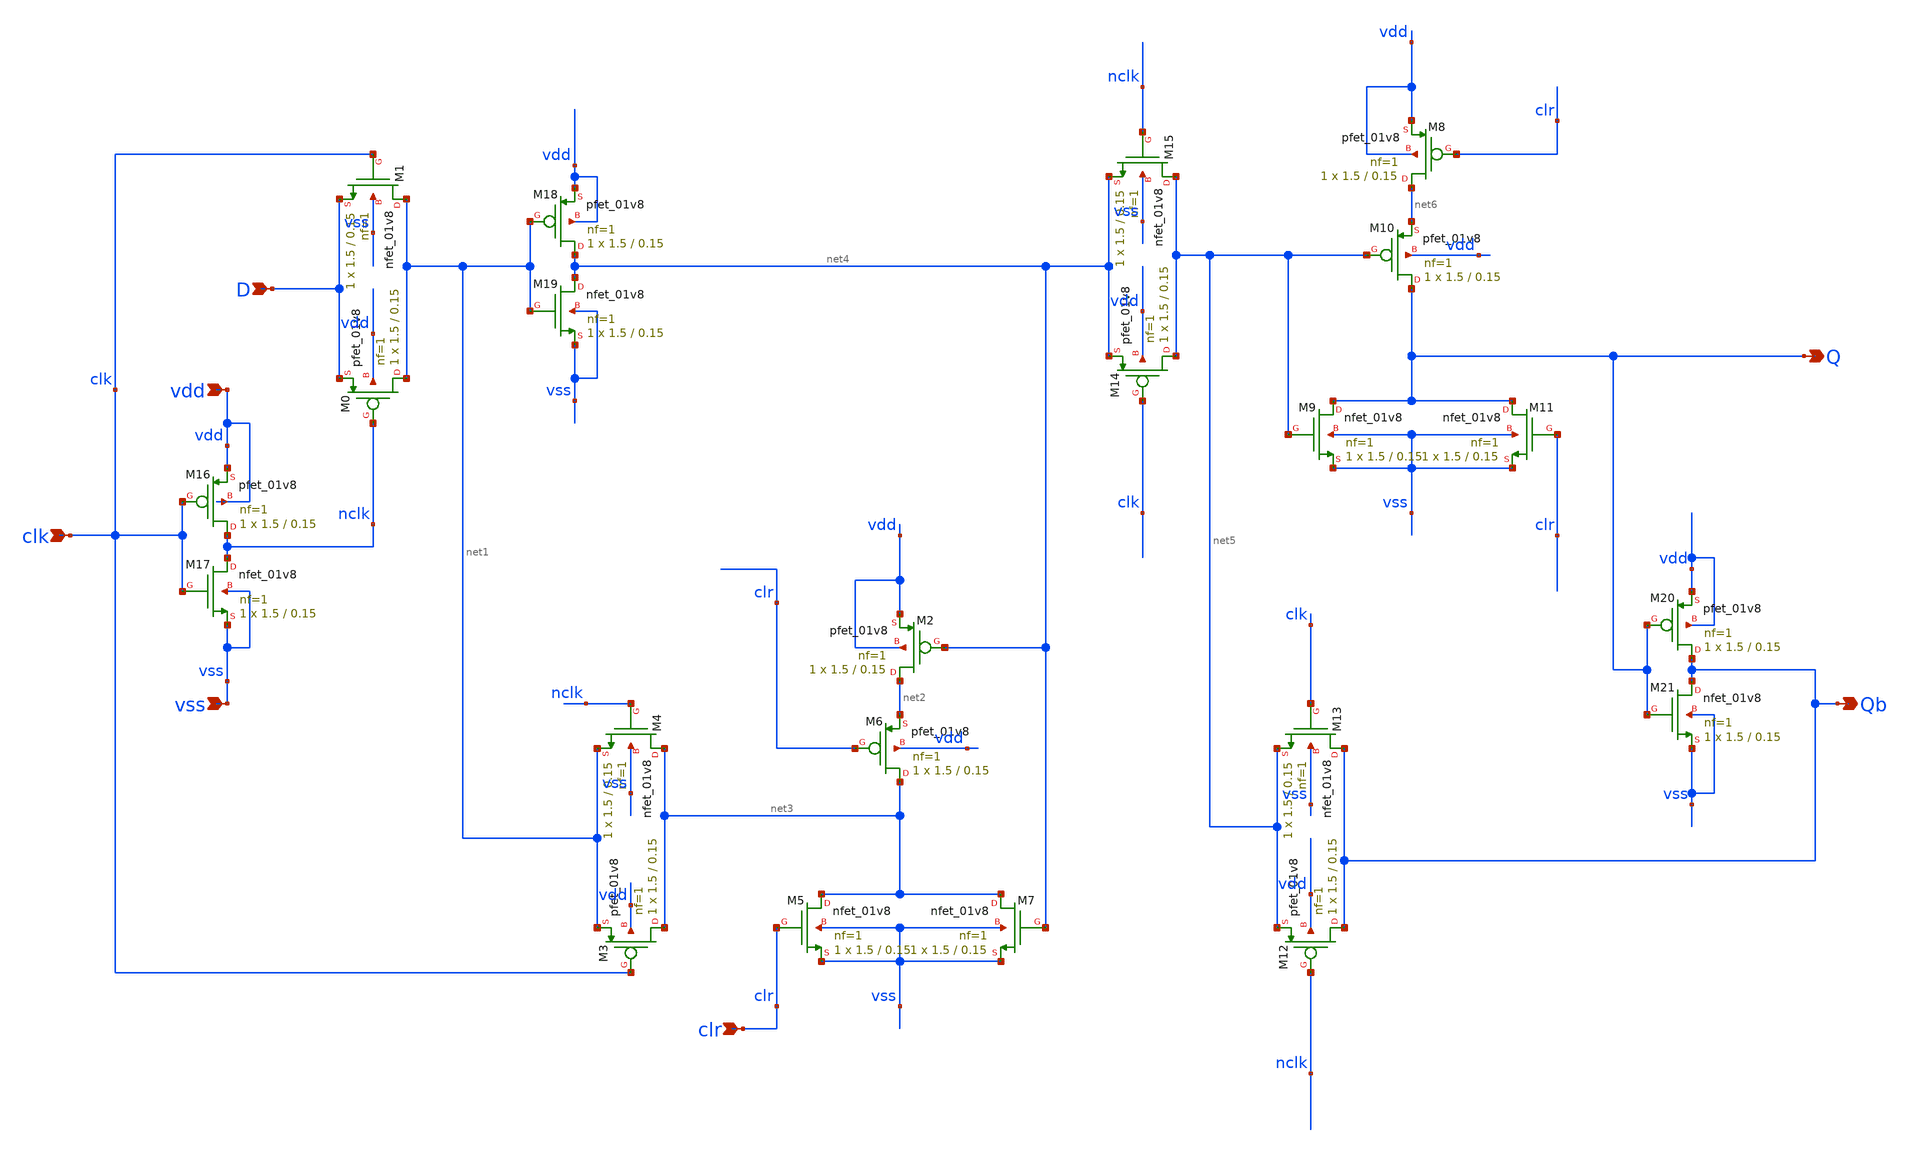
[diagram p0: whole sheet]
** sch_path: track_vlsi/lado/sch/dffc.sch
**.subckt dffc clk vdd vss D Q Qb clr
*.ipin clk
*.ipin vdd
*.ipin vss
*.ipin D
*.opin Q
*.opin Qb
*.ipin clr
XM0 net1 nclk D vdd sky130_fd_pr__pfet_01v8 L=0.15 W=1.5 nf=1 ad='int((nf+1)/2) * W/nf * 0.29' as='int((nf+2)/2) * W/nf * 0.29'
+ pd='2*int((nf+1)/2) * (W/nf + 0.29)' ps='2*int((nf+2)/2) * (W/nf + 0.29)' nrd='0.29 / W' nrs='0.29 / W'
+ sa=0 sb=0 sd=0 mult=1 m=1
XM1 net1 clk D vss sky130_fd_pr__nfet_01v8 L=0.15 W=1.5 nf=1 ad='int((nf+1)/2) * W/nf * 0.29' as='int((nf+2)/2) * W/nf * 0.29'
+ pd='2*int((nf+1)/2) * (W/nf + 0.29)' ps='2*int((nf+2)/2) * (W/nf + 0.29)' nrd='0.29 / W' nrs='0.29 / W'
+ sa=0 sb=0 sd=0 mult=1 m=1
XM2 net2 net4 vdd vdd sky130_fd_pr__pfet_01v8 L=0.15 W=1.5 nf=1 ad='int((nf+1)/2) * W/nf * 0.29' as='int((nf+2)/2) * W/nf * 0.29'
+ pd='2*int((nf+1)/2) * (W/nf + 0.29)' ps='2*int((nf+2)/2) * (W/nf + 0.29)' nrd='0.29 / W' nrs='0.29 / W'
+ sa=0 sb=0 sd=0 mult=1 m=1
XM5 net3 clr vss vss sky130_fd_pr__nfet_01v8 L=0.15 W=1.5 nf=1 ad='int((nf+1)/2) * W/nf * 0.29' as='int((nf+2)/2) * W/nf * 0.29'
+ pd='2*int((nf+1)/2) * (W/nf + 0.29)' ps='2*int((nf+2)/2) * (W/nf + 0.29)' nrd='0.29 / W' nrs='0.29 / W'
+ sa=0 sb=0 sd=0 mult=1 m=1
XM6 net3 clr net2 vdd sky130_fd_pr__pfet_01v8 L=0.15 W=1.5 nf=1 ad='int((nf+1)/2) * W/nf * 0.29' as='int((nf+2)/2) * W/nf * 0.29'
+ pd='2*int((nf+1)/2) * (W/nf + 0.29)' ps='2*int((nf+2)/2) * (W/nf + 0.29)' nrd='0.29 / W' nrs='0.29 / W'
+ sa=0 sb=0 sd=0 mult=1 m=1
XM14 net5 clk net4 vdd sky130_fd_pr__pfet_01v8 L=0.15 W=1.5 nf=1 ad='int((nf+1)/2) * W/nf * 0.29' as='int((nf+2)/2) * W/nf * 0.29'
+ pd='2*int((nf+1)/2) * (W/nf + 0.29)' ps='2*int((nf+2)/2) * (W/nf + 0.29)' nrd='0.29 / W' nrs='0.29 / W'
+ sa=0 sb=0 sd=0 mult=1 m=1
XM15 net5 nclk net4 vss sky130_fd_pr__nfet_01v8 L=0.15 W=1.5 nf=1 ad='int((nf+1)/2) * W/nf * 0.29' as='int((nf+2)/2) * W/nf * 0.29'
+ pd='2*int((nf+1)/2) * (W/nf + 0.29)' ps='2*int((nf+2)/2) * (W/nf + 0.29)' nrd='0.29 / W' nrs='0.29 / W'
+ sa=0 sb=0 sd=0 mult=1 m=1
XM7 net3 net4 vss vss sky130_fd_pr__nfet_01v8 L=0.15 W=1.5 nf=1 ad='int((nf+1)/2) * W/nf * 0.29' as='int((nf+2)/2) * W/nf * 0.29'
+ pd='2*int((nf+1)/2) * (W/nf + 0.29)' ps='2*int((nf+2)/2) * (W/nf + 0.29)' nrd='0.29 / W' nrs='0.29 / W'
+ sa=0 sb=0 sd=0 mult=1 m=1
XM3 net3 clk net1 vdd sky130_fd_pr__pfet_01v8 L=0.15 W=1.5 nf=1 ad='int((nf+1)/2) * W/nf * 0.29' as='int((nf+2)/2) * W/nf * 0.29'
+ pd='2*int((nf+1)/2) * (W/nf + 0.29)' ps='2*int((nf+2)/2) * (W/nf + 0.29)' nrd='0.29 / W' nrs='0.29 / W'
+ sa=0 sb=0 sd=0 mult=1 m=1
XM4 net3 nclk net1 vss sky130_fd_pr__nfet_01v8 L=0.15 W=1.5 nf=1 ad='int((nf+1)/2) * W/nf * 0.29' as='int((nf+2)/2) * W/nf * 0.29'
+ pd='2*int((nf+1)/2) * (W/nf + 0.29)' ps='2*int((nf+2)/2) * (W/nf + 0.29)' nrd='0.29 / W' nrs='0.29 / W'
+ sa=0 sb=0 sd=0 mult=1 m=1
XM8 net6 clr vdd vdd sky130_fd_pr__pfet_01v8 L=0.15 W=1.5 nf=1 ad='int((nf+1)/2) * W/nf * 0.29' as='int((nf+2)/2) * W/nf * 0.29'
+ pd='2*int((nf+1)/2) * (W/nf + 0.29)' ps='2*int((nf+2)/2) * (W/nf + 0.29)' nrd='0.29 / W' nrs='0.29 / W'
+ sa=0 sb=0 sd=0 mult=1 m=1
XM9 Q net5 vss vss sky130_fd_pr__nfet_01v8 L=0.15 W=1.5 nf=1 ad='int((nf+1)/2) * W/nf * 0.29' as='int((nf+2)/2) * W/nf * 0.29'
+ pd='2*int((nf+1)/2) * (W/nf + 0.29)' ps='2*int((nf+2)/2) * (W/nf + 0.29)' nrd='0.29 / W' nrs='0.29 / W'
+ sa=0 sb=0 sd=0 mult=1 m=1
XM10 Q net5 net6 vdd sky130_fd_pr__pfet_01v8 L=0.15 W=1.5 nf=1 ad='int((nf+1)/2) * W/nf * 0.29' as='int((nf+2)/2) * W/nf * 0.29'
+ pd='2*int((nf+1)/2) * (W/nf + 0.29)' ps='2*int((nf+2)/2) * (W/nf + 0.29)' nrd='0.29 / W' nrs='0.29 / W'
+ sa=0 sb=0 sd=0 mult=1 m=1
XM11 Q clr vss vss sky130_fd_pr__nfet_01v8 L=0.15 W=1.5 nf=1 ad='int((nf+1)/2) * W/nf * 0.29' as='int((nf+2)/2) * W/nf * 0.29'
+ pd='2*int((nf+1)/2) * (W/nf + 0.29)' ps='2*int((nf+2)/2) * (W/nf + 0.29)' nrd='0.29 / W' nrs='0.29 / W'
+ sa=0 sb=0 sd=0 mult=1 m=1
XM12 Qb nclk net5 vdd sky130_fd_pr__pfet_01v8 L=0.15 W=1.5 nf=1 ad='int((nf+1)/2) * W/nf * 0.29' as='int((nf+2)/2) * W/nf * 0.29'
+ pd='2*int((nf+1)/2) * (W/nf + 0.29)' ps='2*int((nf+2)/2) * (W/nf + 0.29)' nrd='0.29 / W' nrs='0.29 / W'
+ sa=0 sb=0 sd=0 mult=1 m=1
XM13 Qb clk net5 vss sky130_fd_pr__nfet_01v8 L=0.15 W=1.5 nf=1 ad='int((nf+1)/2) * W/nf * 0.29' as='int((nf+2)/2) * W/nf * 0.29'
+ pd='2*int((nf+1)/2) * (W/nf + 0.29)' ps='2*int((nf+2)/2) * (W/nf + 0.29)' nrd='0.29 / W' nrs='0.29 / W'
+ sa=0 sb=0 sd=0 mult=1 m=1
XM16 nclk clk vdd vdd sky130_fd_pr__pfet_01v8 L=0.15 W=1.5 nf=1 ad='int((nf+1)/2) * W/nf * 0.29' as='int((nf+2)/2) * W/nf * 0.29'
+ pd='2*int((nf+1)/2) * (W/nf + 0.29)' ps='2*int((nf+2)/2) * (W/nf + 0.29)' nrd='0.29 / W' nrs='0.29 / W'
+ sa=0 sb=0 sd=0 mult=1 m=1
XM17 nclk clk vss vss sky130_fd_pr__nfet_01v8 L=0.15 W=1.5 nf=1 ad='int((nf+1)/2) * W/nf * 0.29' as='int((nf+2)/2) * W/nf * 0.29'
+ pd='2*int((nf+1)/2) * (W/nf + 0.29)' ps='2*int((nf+2)/2) * (W/nf + 0.29)' nrd='0.29 / W' nrs='0.29 / W'
+ sa=0 sb=0 sd=0 mult=1 m=1
XM18 net4 net1 vdd vdd sky130_fd_pr__pfet_01v8 L=0.15 W=1.5 nf=1 ad='int((nf+1)/2) * W/nf * 0.29' as='int((nf+2)/2) * W/nf * 0.29'
+ pd='2*int((nf+1)/2) * (W/nf + 0.29)' ps='2*int((nf+2)/2) * (W/nf + 0.29)' nrd='0.29 / W' nrs='0.29 / W'
+ sa=0 sb=0 sd=0 mult=1 m=1
XM19 net4 net1 vss vss sky130_fd_pr__nfet_01v8 L=0.15 W=1.5 nf=1 ad='int((nf+1)/2) * W/nf * 0.29' as='int((nf+2)/2) * W/nf * 0.29'
+ pd='2*int((nf+1)/2) * (W/nf + 0.29)' ps='2*int((nf+2)/2) * (W/nf + 0.29)' nrd='0.29 / W' nrs='0.29 / W'
+ sa=0 sb=0 sd=0 mult=1 m=1
XM20 Qb Q vdd vdd sky130_fd_pr__pfet_01v8 L=0.15 W=1.5 nf=1 ad='int((nf+1)/2) * W/nf * 0.29' as='int((nf+2)/2) * W/nf * 0.29'
+ pd='2*int((nf+1)/2) * (W/nf + 0.29)' ps='2*int((nf+2)/2) * (W/nf + 0.29)' nrd='0.29 / W' nrs='0.29 / W'
+ sa=0 sb=0 sd=0 mult=1 m=1
XM21 Qb Q vss vss sky130_fd_pr__nfet_01v8 L=0.15 W=1.5 nf=1 ad='int((nf+1)/2) * W/nf * 0.29' as='int((nf+2)/2) * W/nf * 0.29'
+ pd='2*int((nf+1)/2) * (W/nf + 0.29)' ps='2*int((nf+2)/2) * (W/nf + 0.29)' nrd='0.29 / W' nrs='0.29 / W'
+ sa=0 sb=0 sd=0 mult=1 m=1
**.ends
.end
